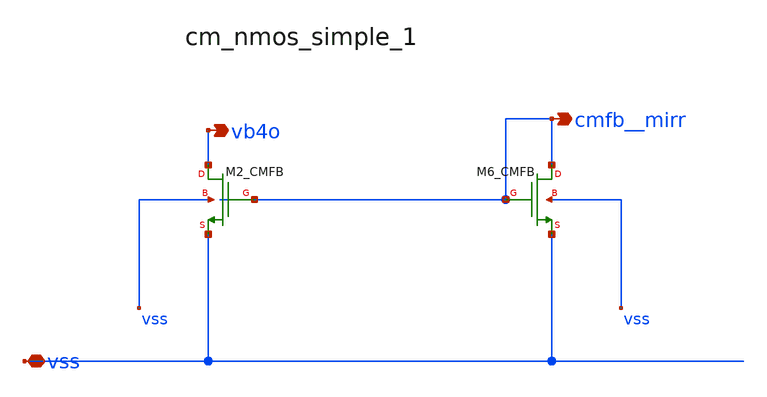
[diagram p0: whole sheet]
** sch_path: analog-db/raw/ia_006_fan_chopper_cmfb/hier/blocks/cm_nmos_simple_1.sch
**.subckt cm_nmos_simple_1 vss vb4o cmfb__mirr
*.iopin vss
*.opin vb4o
*.opin cmfb__mirr
XM2_CMFB vb4o cmfb__mirr vss vss sg13_lv_nmos w=x_dut_xm2_cmfb_w l=x_dut_xm2_cmfb_l ng=1
+ m=x_dut_xm2_cmfb_m
XM6_CMFB cmfb__mirr cmfb__mirr vss vss sg13_lv_nmos w=x_dut_xm6_cmfb_w l=x_dut_xm6_cmfb_l ng=1
+ m=x_dut_xm6_cmfb_m
**.ends
.end
